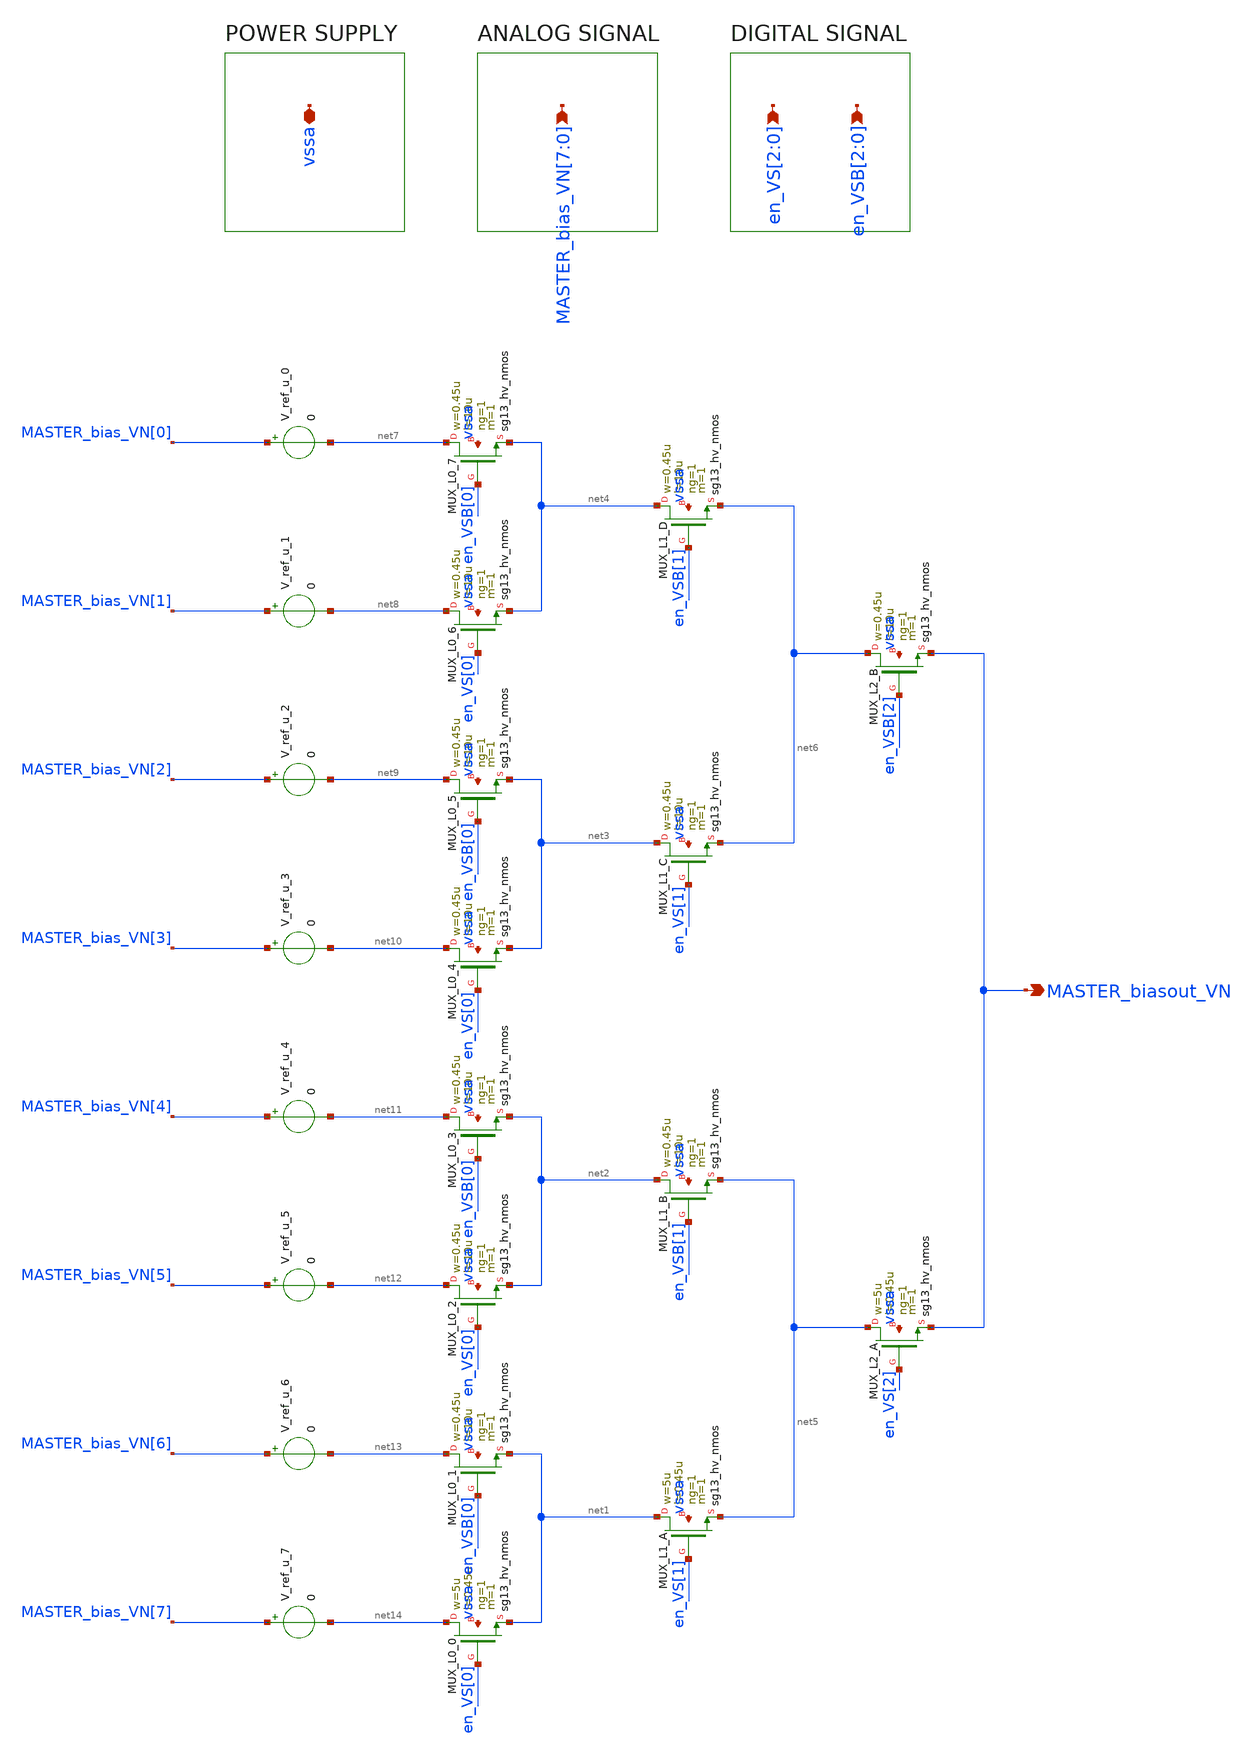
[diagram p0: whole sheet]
** sch_path: SelMUX.sch
**.subckt SelMUX
*+ MASTER_bias_VN[7],MASTER_bias_VN[6],MASTER_bias_VN[5],MASTER_bias_VN[4],MASTER_bias_VN[3],MASTER_bias_VN[2],MASTER_bias_VN[1],MASTER_bias_VN[0] MASTER_biasout_VN en_VS[2],en_VS[1],en_VS[0] en_VSB[2],en_VSB[1],en_VSB[0] vssa
*.ipin
*+ MASTER_bias_VN[7],MASTER_bias_VN[6],MASTER_bias_VN[5],MASTER_bias_VN[4],MASTER_bias_VN[3],MASTER_bias_VN[2],MASTER_bias_VN[1],MASTER_bias_VN[0]
*.opin MASTER_biasout_VN
*.ipin en_VS[2],en_VS[1],en_VS[0]
*.ipin en_VSB[2],en_VSB[1],en_VSB[0]
*.iopin vssa
XMUX_L0_0 net14 en_VS[0] net1 vssa sg13_hv_nmos w=5u l=0.45u ng=1 m=1 mm_ok=1
XMUX_L0_1 net13 en_VSB[0] net1 vssa sg13_hv_nmos w=0.45u l=10u ng=1 m=1 mm_ok=1
XMUX_L0_2 net12 en_VS[0] net2 vssa sg13_hv_nmos w=0.45u l=10u ng=1 m=1 mm_ok=1
XMUX_L0_3 net11 en_VSB[0] net2 vssa sg13_hv_nmos w=0.45u l=10u ng=1 m=1 mm_ok=1
XMUX_L0_4 net10 en_VS[0] net3 vssa sg13_hv_nmos w=0.45u l=10u ng=1 m=1 mm_ok=1
XMUX_L0_5 net9 en_VSB[0] net3 vssa sg13_hv_nmos w=0.45u l=10u ng=1 m=1 mm_ok=1
XMUX_L0_6 net8 en_VS[0] net4 vssa sg13_hv_nmos w=0.45u l=10u ng=1 m=1 mm_ok=1
XMUX_L0_7 net7 en_VSB[0] net4 vssa sg13_hv_nmos w=0.45u l=10u ng=1 m=1 mm_ok=1
XMUX_L1_A net1 en_VS[1] net5 vssa sg13_hv_nmos w=5u l=0.45u ng=1 m=1 mm_ok=1
XMUX_L1_B net2 en_VSB[1] net5 vssa sg13_hv_nmos w=0.45u l=10u ng=1 m=1 mm_ok=1
XMUX_L1_C net3 en_VS[1] net6 vssa sg13_hv_nmos w=0.45u l=10u ng=1 m=1 mm_ok=1
XMUX_L1_D net4 en_VSB[1] net6 vssa sg13_hv_nmos w=0.45u l=10u ng=1 m=1 mm_ok=1
XMUX_L2_A net5 en_VS[2] MASTER_biasout_VN vssa sg13_hv_nmos w=5u l=0.45u ng=1 m=1 mm_ok=1
XMUX_L2_B net6 en_VSB[2] MASTER_biasout_VN vssa sg13_hv_nmos w=0.45u l=10u ng=1 m=1 mm_ok=1
V_ref_u_0 MASTER_bias_VN[0] net7 0
V_ref_u_1 MASTER_bias_VN[1] net8 0
V_ref_u_2 MASTER_bias_VN[2] net9 0
V_ref_u_3 MASTER_bias_VN[3] net10 0
V_ref_u_4 MASTER_bias_VN[4] net11 0
V_ref_u_5 MASTER_bias_VN[5] net12 0
V_ref_u_6 MASTER_bias_VN[6] net13 0
V_ref_u_7 MASTER_bias_VN[7] net14 0
**.ends
.end
